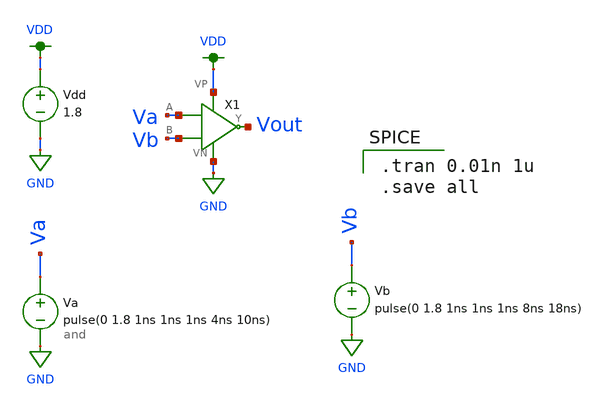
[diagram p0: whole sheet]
** sch_path: 1_And_Gate/and_test.sch
**.subckt and_test
Vdd VDD GND 1.8
Va Va GND pulse(0 1.8 1ns 1ns 1ns 4ns 10ns)
Vb Vb GND pulse(0 1.8 1ns 1ns 1ns 8ns 18ns)
X1 Va Vout VDD GND Vb and
**** begin user architecture code

.tran 0.01n 1u
.save all


.option wnflag=1
.lib ~/skywater/skywater-pdk/libraries/sky130_fd_pr_ngspice/latest/models/sky130.lib.spice tt

**** end user architecture code
**.ends
.GLOBAL VDD
.GLOBAL GND
.end
